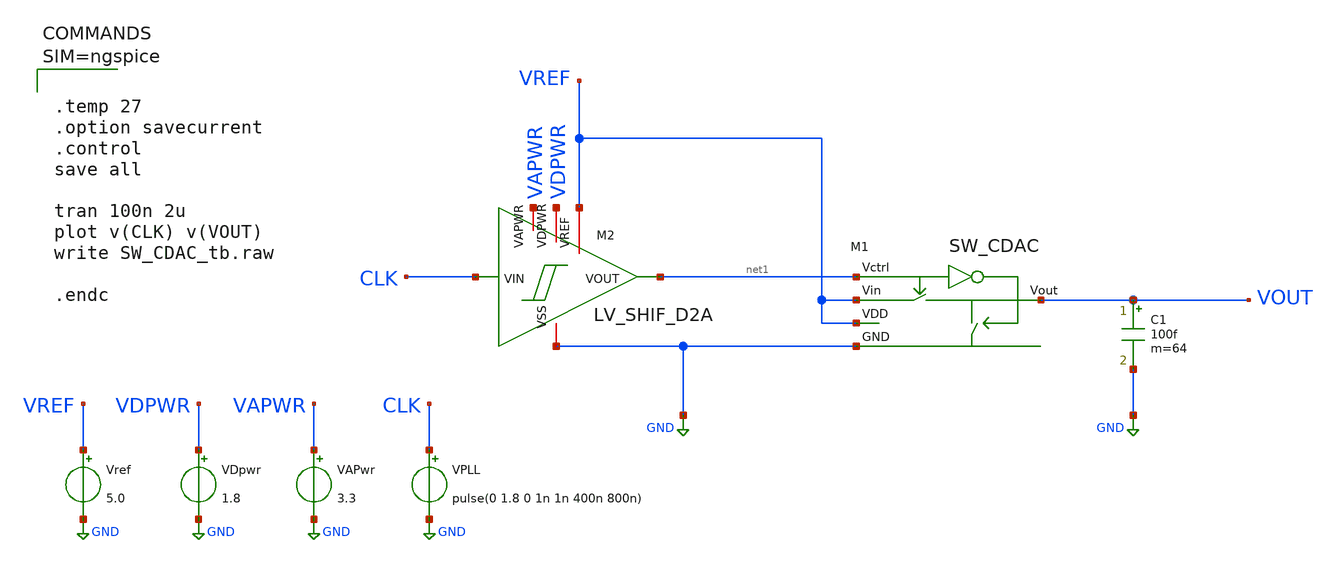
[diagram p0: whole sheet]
** sch_path: SKY130/SAR-ADC/SAR-ADC_5.0V/SW_CDAC_tb.sch
**.subckt SW_CDAC_tb
VAPwr VAPWR GND 3.3
Vref VREF GND 5.0
VDpwr VDPWR GND 1.8
XM1 VREF net1 GND VOUT VREF SW_CDAC
XM2 VAPWR VDPWR VREF net1 CLK GND LV_SHIF_D2A
VPLL CLK GND pulse(0 1.8 0 1n 1n 400n 800n)
C1 VOUT GND 100f m=64
**** begin user architecture code



.temp 27
.option savecurrent
.control
save all

tran 100n 2u
plot v(CLK) v(VOUT)
write SW_CDAC_tb.raw

.endc




** opencircuitdesign pdks install
.lib $::SKYWATER_MODELS/sky130.lib.spice tt

**** end user architecture code
**.ends
.GLOBAL GND
.end
